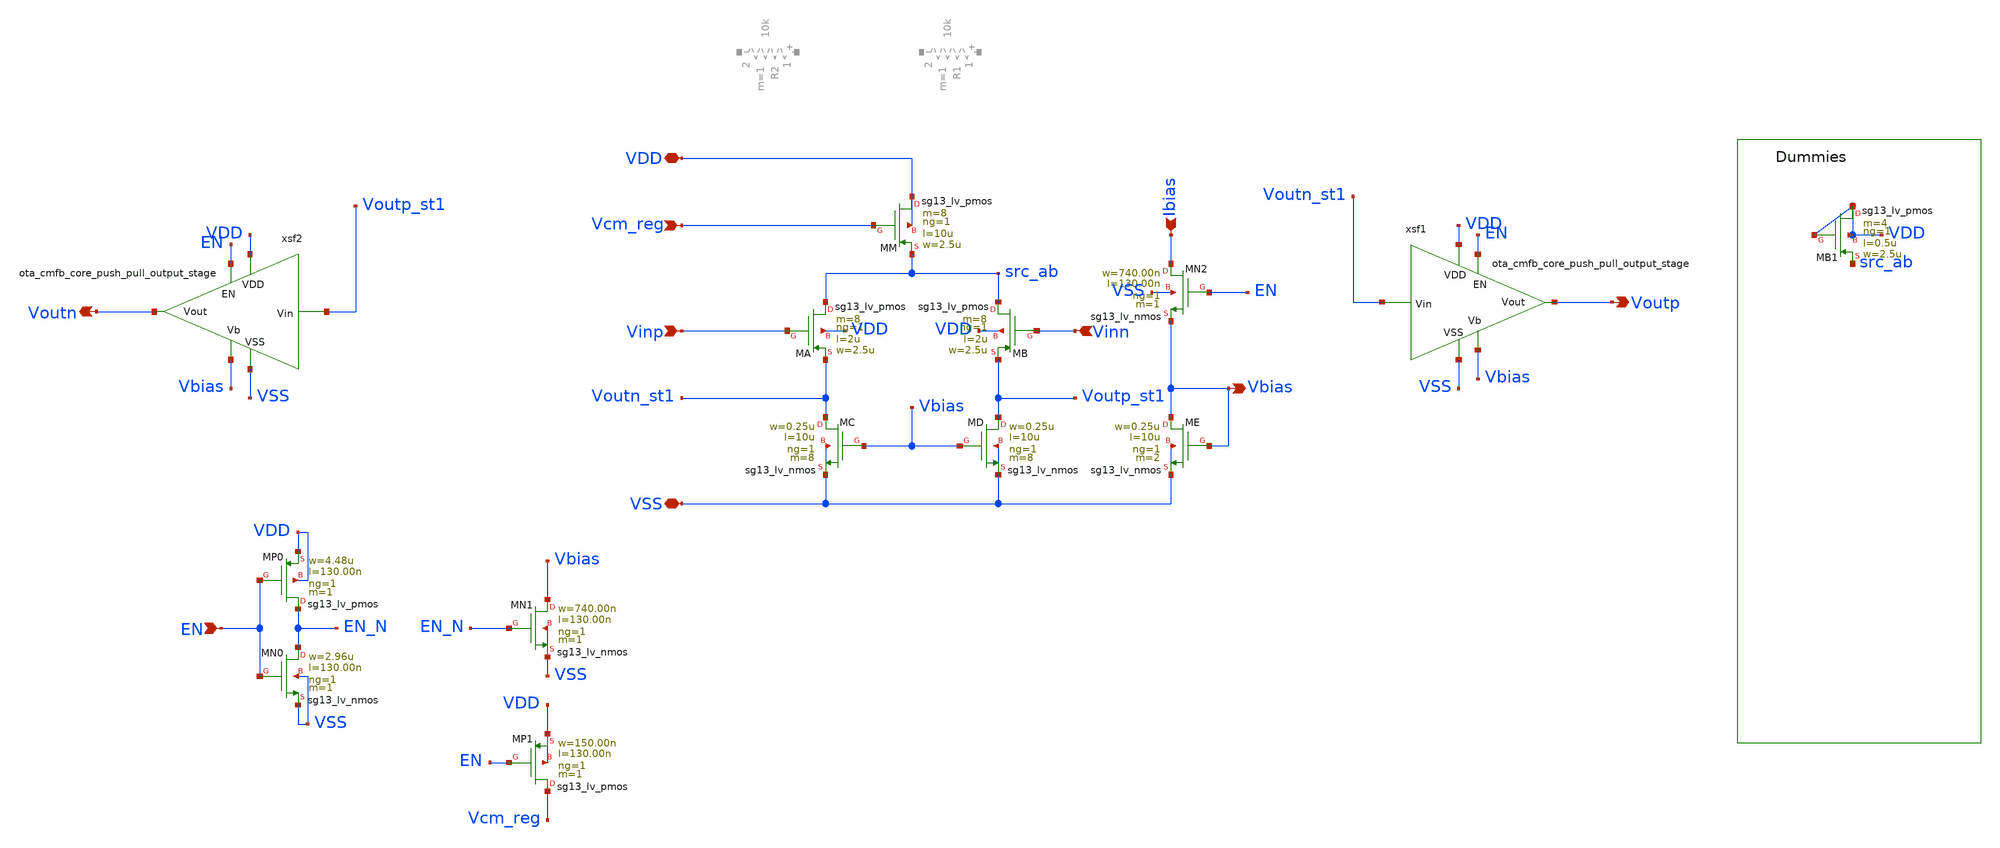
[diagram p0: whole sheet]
** sch_path: schema/ota_cmfb_core/ota_cmfb_core.sch
**.subckt ota_cmfb_core Voutn Voutp VDD VSS Vinp Ibias Vinn Vcm_reg EN Vbias
*.opin Voutn
*.opin Voutp
*.iopin VDD
*.iopin VSS
*.ipin Vinp
*.ipin Ibias
*.ipin Vinn
*.ipin Vcm_reg
*.ipin EN
*.opin Vbias
XMD Voutp_st1 Vbias VSS VSS sg13_lv_nmos w=0.25u l=10u ng=1 m=8 mm_ok=1
XMB src_ab Vinn Voutp_st1 VDD sg13_lv_pmos w=2.5u l=2u ng=1 m=8 mm_ok=1
XMC Voutn_st1 Vbias VSS VSS sg13_lv_nmos w=0.25u l=10u ng=1 m=8 mm_ok=1
XMA src_ab Vinp Voutn_st1 VDD sg13_lv_pmos w=2.5u l=2u ng=1 m=8 mm_ok=1
XMM VDD Vcm_reg src_ab VDD sg13_lv_pmos w=2.5u l=10u ng=1 m=8 mm_ok=1
XME Vbias Vbias VSS VSS sg13_lv_nmos w=0.25u l=10u ng=1 m=2 mm_ok=1
xsf1 VDD Voutn_st1 Voutp Vbias VSS EN ota_cmfb_core_push_pull_output_stage
xsf2 VDD Voutp_st1 Voutn Vbias VSS EN ota_cmfb_core_push_pull_output_stage
XMN0 EN_N EN VSS VSS sg13_lv_nmos w=2.96u l=130.00n ng=1 m=1 mm_ok=1
XMP0 EN_N EN VDD VDD sg13_lv_pmos w=4.48u l=130.00n ng=1 m=1 mm_ok=1
XMN1 Vbias EN_N VSS VSS sg13_lv_nmos w=740.00n l=130.00n ng=1 m=1 mm_ok=1
XMP1 Vcm_reg EN VDD VDD sg13_lv_pmos w=150.00n l=130.00n ng=1 m=1 mm_ok=1
XMB1 VDD VDD src_ab VDD sg13_lv_pmos w=2.5u l=0.5u ng=1 m=4 mm_ok=1
XMN2 Ibias EN Vbias VSS sg13_lv_nmos w=740.00n l=130.00n ng=1 m=1 mm_ok=1
**.ends

* expanding   symbol:  ota_cmfb_core/ota_cmfb_core_push_pull_output_stage.sym # of pins=6
** sym_path: schema/ota_cmfb_core/ota_cmfb_core_push_pull_output_stage.sym
** sch_path: schema/ota_cmfb_core/ota_cmfb_core_push_pull_output_stage.sch
.subckt ota_cmfb_core_push_pull_output_stage VDD Vin Vout Vbias VSS EN
*.iopin VSS
*.iopin VDD
*.ipin Vbias
*.ipin Vin
*.opin Vout
*.ipin EN
XM1 Vout Vin_shifted VSS VSS sg13_lv_nmos w=0.5u l=10u ng=1 m=1 mm_ok=1
XM2 VDD Vin Vout VDD sg13_lv_pmos w=5u l=0.5u ng=1 m=1 mm_ok=1
XMC VDD Vbiasp CD_DRN VDD sg13_lv_pmos w=2.5u l=3u ng=1 m=4 mm_ok=1
XME Vin_shifted Vcasp2 Vin VDD sg13_lv_pmos w=2.5u l=3u ng=1 m=2 mm_ok=1
XMD CD_DRN Vcasp Vin VDD sg13_lv_pmos w=2.5u l=3u ng=1 m=4 mm_ok=1
XMN Vin Vcasn2 Vin_shifted VSS sg13_lv_nmos w=0.7u l=3u ng=1 m=2 mm_ok=1
XMH VDD Vbiasp net1 VDD sg13_lv_pmos w=2.5u l=3u ng=1 m=4 mm_ok=1
XMI net1 Vcasp Vcasp VDD sg13_lv_pmos w=2.5u l=3u ng=1 m=4 mm_ok=1
XMJ Vcasp Vcasp2 Vcasp2 VDD sg13_lv_pmos w=2.5u l=3u ng=1 m=4 mm_ok=1
XMB VDD Vbiasp Vcasn2 VDD sg13_lv_pmos w=2.5u l=3u ng=1 m=4 mm_ok=1
XMO Vcasn2 Vcasn2 Vcasn VSS sg13_lv_nmos w=0.7u l=3u ng=1 m=4 mm_ok=1
XR1 net2 Vout VSS rhigh w=0.5e-6 l=1e-6*8 m=1 b=0 mm_ok=1
XC1 Vin net2 sg13_moscap_p w=3.5u l=21.5u m=1 mm_ok=1
XMFG Vbiasp Vbias VSS VSS sg13_lv_nmos w=0.25u l=10u ng=1 m=2 mm_ok=1
XMA VDD Vbiasp Vbiasp VDD sg13_lv_pmos w=2.5u l=3u ng=1 m=10 mm_ok=1
XMP Vcasn Vcasn Vbiasn VSS sg13_lv_nmos w=0.7u l=3u ng=1 m=4 mm_ok=1
XMQ Vbiasn Vbiasn VSS VSS sg13_lv_nmos w=0.7u l=3u ng=1 m=4 mm_ok=1
XMM Vin_shifted Vcasn src_ml VSS sg13_lv_nmos w=0.7u l=3u ng=1 m=4 mm_ok=1
XML src_ml Vbiasn VSS VSS sg13_lv_nmos w=0.7u l=3u ng=1 m=4 mm_ok=1
XMK Vcasp2 Vbiasn VSS VSS sg13_lv_nmos w=0.7u l=3u ng=1 m=4 mm_ok=1
XM3 CD_DRN VDD VDD VDD sg13_lv_pmos w=2.5u l=0.5u ng=1 m=2 mm_ok=1
XM4 Vin_shifted VDD VDD VDD sg13_lv_pmos w=2.5u l=0.5u ng=1 m=1 mm_ok=1
XM5 Vbiasp VDD VDD VDD sg13_lv_pmos w=2.5u l=0.5u ng=1 m=1 mm_ok=1
XM6 Vin VDD VDD VDD sg13_lv_pmos w=2.5u l=0.5u ng=1 m=1 mm_ok=1
XM7 VSS VSS Vin_shifted VSS sg13_lv_nmos w=0.7u l=0.5u ng=1 m=2 mm_ok=1
XM8 VSS VSS Vcasn VSS sg13_lv_nmos w=0.7u l=0.5u ng=1 m=4 mm_ok=1
XMX VSS VSS Vin_shifted VSS sg13_lv_nmos w=0.7u l=3u ng=1 m=4 mm_ok=1
XM9 VSS VSS src_ml VSS sg13_lv_nmos w=0.7u l=0.5u ng=1 m=4 mm_ok=1
XM10 Vcasp VDD VDD VDD sg13_lv_pmos w=2.5u l=0.5u ng=1 m=2 mm_ok=1
XM12 VSS VSS Vbiasp VSS sg13_lv_nmos w=0.25u l=0.5u ng=1 m=2 mm_ok=1
XM13 Vbiasp EN VDD VDD sg13_lv_pmos w=0.15u l=0.13u ng=1 m=1 mm_ok=1
XMN0 EN_N EN VSS VSS sg13_lv_nmos w=2.96u l=130.00n ng=1 m=1 mm_ok=1
XMP0 EN_N EN VDD VDD sg13_lv_pmos w=4.48u l=130.00n ng=1 m=1 mm_ok=1
XMN1 Vbiasn EN_N VSS VSS sg13_lv_nmos w=740.00n l=130.00n ng=1 m=1 mm_ok=1
XM14 Vin EN VDD VDD sg13_lv_pmos w=0.15u l=0.13u ng=1 m=1 mm_ok=1
.ends

.end
